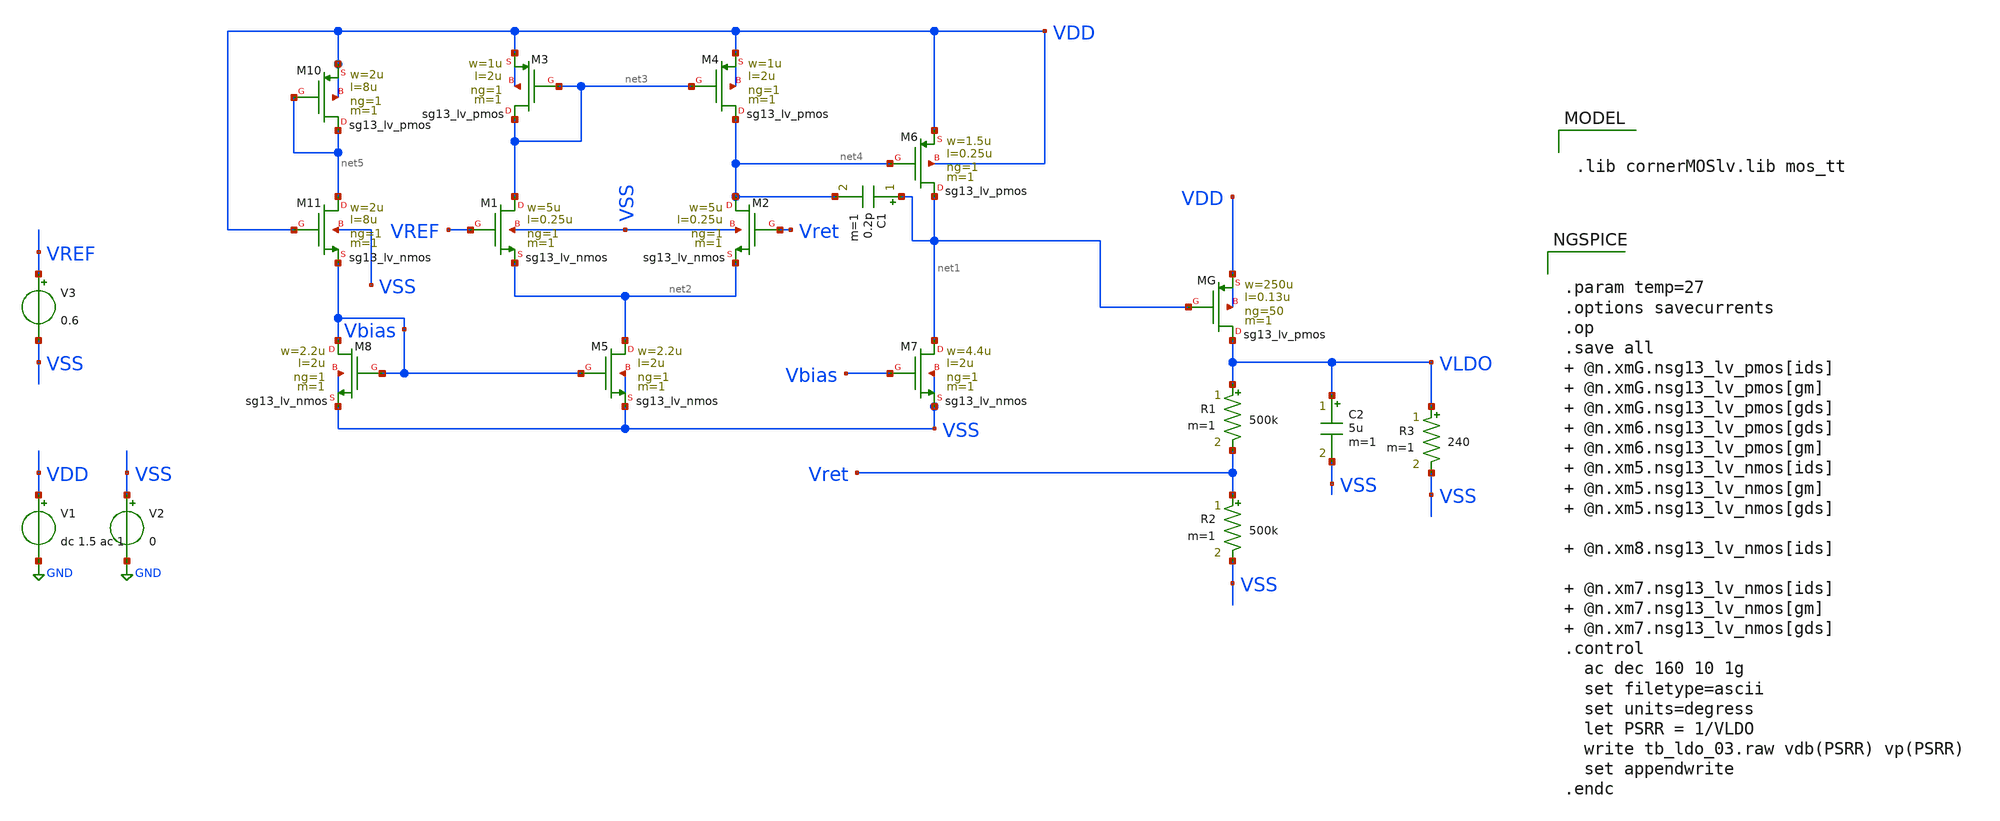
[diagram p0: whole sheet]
** sch_path: designs/1iee34/LDO.sch
**.subckt LDO
V1 VDD GND dc 1.5 ac 1
V2 VSS GND 0
V3 VREF VSS 0.6
XMG VLDO net1 VDD VDD sg13_lv_pmos w=250u l=0.13u ng=50 m=1 mm_ok=1
R2 Vret VSS 500k m=1
R1 VLDO Vret 500k m=1
R3 VLDO VSS 240 m=1
XM1 net3 VREF net2 VSS sg13_lv_nmos w=5u l=0.25u ng=1 m=1 mm_ok=1
XM2 net4 Vret net2 VSS sg13_lv_nmos w=5u l=0.25u ng=1 m=1 mm_ok=1
XM3 net3 net3 VDD VDD sg13_lv_pmos w=1u l=2u ng=1 m=1 mm_ok=1
XM4 net4 net3 VDD VDD sg13_lv_pmos w=1u l=2u ng=1 m=1 mm_ok=1
XM5 net2 Vbias VSS VSS sg13_lv_nmos w=2.2u l=2u ng=1 m=1 mm_ok=1
XM8 Vbias Vbias VSS VSS sg13_lv_nmos w=2.2u l=2u ng=1 m=1 mm_ok=1
XM7 net1 Vbias VSS VSS sg13_lv_nmos w=4.4u l=2u ng=1 m=1 mm_ok=1
XM6 net1 net4 VDD VDD sg13_lv_pmos w=1.5u l=0.25u ng=1 m=1 mm_ok=1
C1 net1 net4 0.2p m=1
C2 VLDO VSS 5u m=1
XM10 net5 net5 VDD VDD sg13_lv_pmos w=2u l=8u ng=1 m=1 mm_ok=1
XM11 net5 VDD Vbias VSS sg13_lv_nmos w=2u l=8u ng=1 m=1 mm_ok=1
**** begin user architecture code


.param temp=27
.options savecurrents
.op
.save all  @n.xmG.nsg13_lv_pmos[ids]  @n.xmG.nsg13_lv_pmos[gm]  @n.xmG.nsg13_lv_pmos[gds]  @n.xm6.nsg13_lv_pmos[gds]  @n.xm6.nsg13_lv_pmos[gm]  @n.xm5.nsg13_lv_nmos[ids]  @n.xm5.nsg13_lv_nmos[gm]  @n.xm5.nsg13_lv_nmos[gds]
  @n.xm8.nsg13_lv_nmos[ids]
  @n.xm7.nsg13_lv_nmos[ids]  @n.xm7.nsg13_lv_nmos[gm]  @n.xm7.nsg13_lv_nmos[gds]
.control
  ac dec 160 10 1g
  set filetype=ascii
  set units=degress
  let PSRR = 1/VLDO
  write tb_ldo_03.raw vdb(PSRR) vp(PSRR)
  set appendwrite
.endc




.lib cornerMOSlv.lib mos_tt


**** end user architecture code
**.ends
.GLOBAL GND
.end
